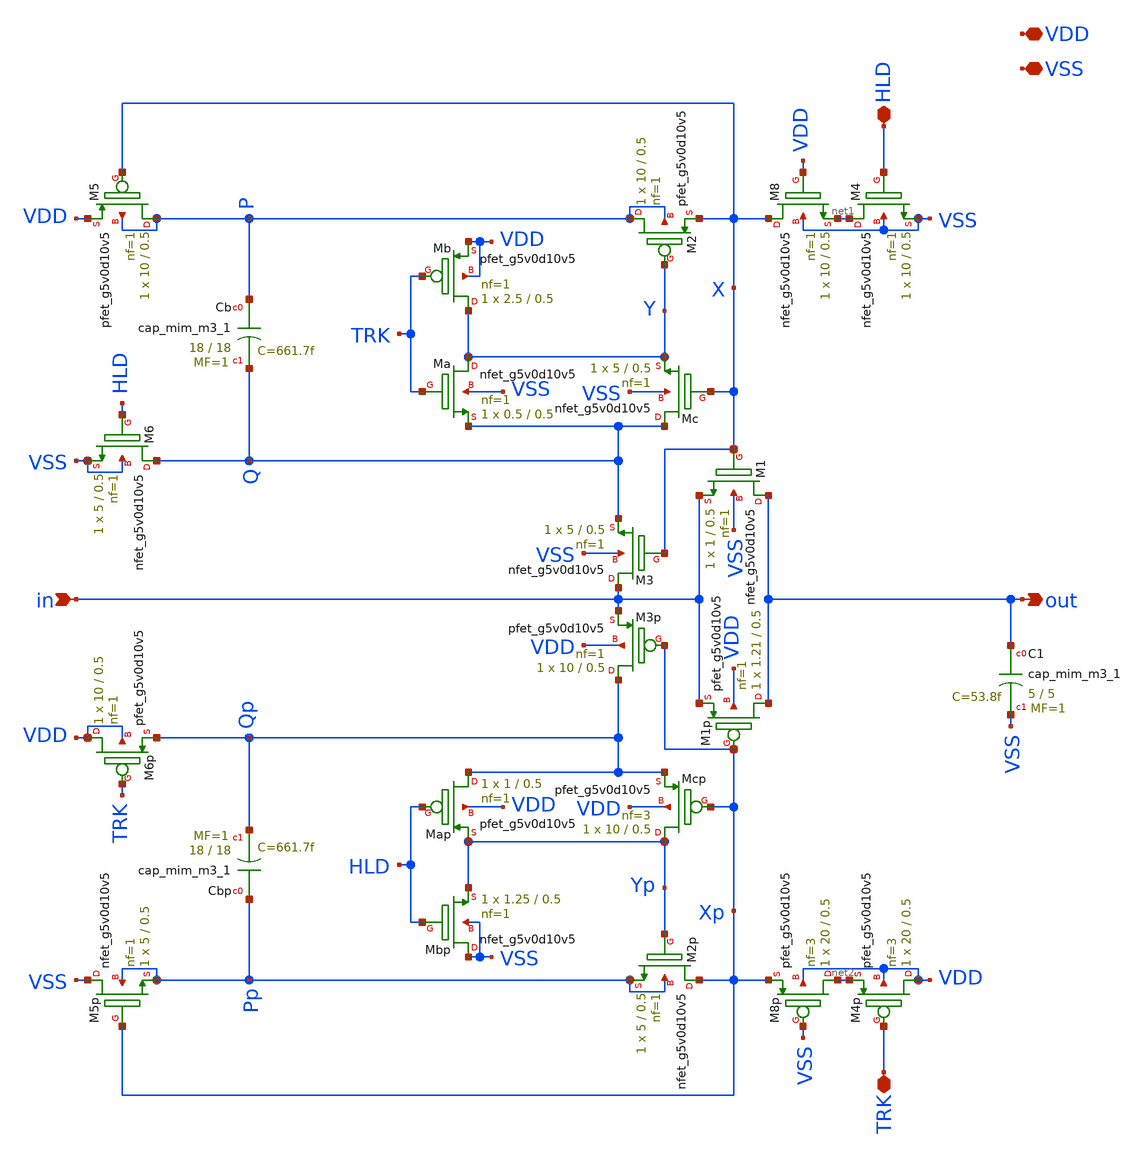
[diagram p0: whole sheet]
** sch_path: xschem/track_and_hold/track_and_hold.sch
**.subckt track_and_hold VSS VDD in out HLD TRK
*.iopin VSS
*.iopin VDD
*.ipin in
*.opin out
*.iopin HLD
*.iopin TRK
XC1 out VSS sky130_fd_pr__cap_mim_m3_1 W=5 L=5 MF=1 m=1
XM1 out X in VSS sky130_fd_pr__nfet_g5v0d10v5 L=0.5 W=1 nf=1 ad='int((nf+1)/2) * W/nf * 0.29' as='int((nf+2)/2) * W/nf * 0.29'
+ pd='2*int((nf+1)/2) * (W/nf + 0.29)' ps='2*int((nf+2)/2) * (W/nf + 0.29)' nrd='0.29 / W' nrs='0.29 / W'
+ sa=0 sb=0 sd=0 mult=1 m=1
XM1p out Xp in VDD sky130_fd_pr__pfet_g5v0d10v5 L=0.5 W=1.21 nf=1 ad='int((nf+1)/2) * W/nf * 0.29' as='int((nf+2)/2) * W/nf * 0.29'
+ pd='2*int((nf+1)/2) * (W/nf + 0.29)' ps='2*int((nf+2)/2) * (W/nf + 0.29)' nrd='0.29 / W' nrs='0.29 / W'
+ sa=0 sb=0 sd=0 mult=1 m=1
XM4 net1 HLD VSS VSS sky130_fd_pr__nfet_g5v0d10v5 L=0.5 W=10 nf=1 ad='int((nf+1)/2) * W/nf * 0.29' as='int((nf+2)/2) * W/nf * 0.29'
+ pd='2*int((nf+1)/2) * (W/nf + 0.29)' ps='2*int((nf+2)/2) * (W/nf + 0.29)' nrd='0.29 / W' nrs='0.29 / W'
+ sa=0 sb=0 sd=0 mult=1 m=1
XM2 P Y X P sky130_fd_pr__pfet_g5v0d10v5 L=0.5 W=10 nf=1 ad='int((nf+1)/2) * W/nf * 0.29' as='int((nf+2)/2) * W/nf * 0.29'
+ pd='2*int((nf+1)/2) * (W/nf + 0.29)' ps='2*int((nf+2)/2) * (W/nf + 0.29)' nrd='0.29 / W' nrs='0.29 / W'
+ sa=0 sb=0 sd=0 mult=1 m=1
XM3 in X Q VSS sky130_fd_pr__nfet_g5v0d10v5 L=0.5 W=5 nf=1 ad='int((nf+1)/2) * W/nf * 0.29' as='int((nf+2)/2) * W/nf * 0.29'
+ pd='2*int((nf+1)/2) * (W/nf + 0.29)' ps='2*int((nf+2)/2) * (W/nf + 0.29)' nrd='0.29 / W' nrs='0.29 / W'
+ sa=0 sb=0 sd=0 mult=1 m=1
XM6 Q HLD VSS VSS sky130_fd_pr__nfet_g5v0d10v5 L=0.5 W=5 nf=1 ad='int((nf+1)/2) * W/nf * 0.29' as='int((nf+2)/2) * W/nf * 0.29'
+ pd='2*int((nf+1)/2) * (W/nf + 0.29)' ps='2*int((nf+2)/2) * (W/nf + 0.29)' nrd='0.29 / W' nrs='0.29 / W'
+ sa=0 sb=0 sd=0 mult=1 m=1
XM3p Qp Xp in VDD sky130_fd_pr__pfet_g5v0d10v5 L=0.5 W=10 nf=1 ad='int((nf+1)/2) * W/nf * 0.29' as='int((nf+2)/2) * W/nf * 0.29'
+ pd='2*int((nf+1)/2) * (W/nf + 0.29)' ps='2*int((nf+2)/2) * (W/nf + 0.29)' nrd='0.29 / W' nrs='0.29 / W'
+ sa=0 sb=0 sd=0 mult=1 m=1
XM5 P X VDD P sky130_fd_pr__pfet_g5v0d10v5 L=0.5 W=10 nf=1 ad='int((nf+1)/2) * W/nf * 0.29' as='int((nf+2)/2) * W/nf * 0.29'
+ pd='2*int((nf+1)/2) * (W/nf + 0.29)' ps='2*int((nf+2)/2) * (W/nf + 0.29)' nrd='0.29 / W' nrs='0.29 / W'
+ sa=0 sb=0 sd=0 mult=1 m=1
XCb P Q sky130_fd_pr__cap_mim_m3_1 W=18 L=18 MF=1 m=1
XM8 X VDD net1 VSS sky130_fd_pr__nfet_g5v0d10v5 L=0.5 W=10 nf=1 ad='int((nf+1)/2) * W/nf * 0.29' as='int((nf+2)/2) * W/nf * 0.29'
+ pd='2*int((nf+1)/2) * (W/nf + 0.29)' ps='2*int((nf+2)/2) * (W/nf + 0.29)' nrd='0.29 / W' nrs='0.29 / W'
+ sa=0 sb=0 sd=0 mult=1 m=1
XMb Y TRK VDD VDD sky130_fd_pr__pfet_g5v0d10v5 L=0.5 W=2.5 nf=1 ad='int((nf+1)/2) * W/nf * 0.29' as='int((nf+2)/2) * W/nf * 0.29'
+ pd='2*int((nf+1)/2) * (W/nf + 0.29)' ps='2*int((nf+2)/2) * (W/nf + 0.29)' nrd='0.29 / W' nrs='0.29 / W'
+ sa=0 sb=0 sd=0 mult=1 m=1
XMa Y TRK Q VSS sky130_fd_pr__nfet_g5v0d10v5 L=0.5 W=0.5 nf=1 ad='int((nf+1)/2) * W/nf * 0.29' as='int((nf+2)/2) * W/nf * 0.29'
+ pd='2*int((nf+1)/2) * (W/nf + 0.29)' ps='2*int((nf+2)/2) * (W/nf + 0.29)' nrd='0.29 / W' nrs='0.29 / W'
+ sa=0 sb=0 sd=0 mult=1 m=1
XMc Q X Y VSS sky130_fd_pr__nfet_g5v0d10v5 L=0.5 W=5 nf=1 ad='int((nf+1)/2) * W/nf * 0.29' as='int((nf+2)/2) * W/nf * 0.29'
+ pd='2*int((nf+1)/2) * (W/nf + 0.29)' ps='2*int((nf+2)/2) * (W/nf + 0.29)' nrd='0.29 / W' nrs='0.29 / W'
+ sa=0 sb=0 sd=0 mult=1 m=1
XCbp Pp Qp sky130_fd_pr__cap_mim_m3_1 W=18 L=18 MF=1 m=1
XM6p VDD TRK Qp VDD sky130_fd_pr__pfet_g5v0d10v5 L=0.5 W=10 nf=1 ad='int((nf+1)/2) * W/nf * 0.29' as='int((nf+2)/2) * W/nf * 0.29'
+ pd='2*int((nf+1)/2) * (W/nf + 0.29)' ps='2*int((nf+2)/2) * (W/nf + 0.29)' nrd='0.29 / W' nrs='0.29 / W'
+ sa=0 sb=0 sd=0 mult=1 m=1
XM5p VSS Xp Pp Pp sky130_fd_pr__nfet_g5v0d10v5 L=0.5 W=5 nf=1 ad='int((nf+1)/2) * W/nf * 0.29' as='int((nf+2)/2) * W/nf * 0.29'
+ pd='2*int((nf+1)/2) * (W/nf + 0.29)' ps='2*int((nf+2)/2) * (W/nf + 0.29)' nrd='0.29 / W' nrs='0.29 / W'
+ sa=0 sb=0 sd=0 mult=1 m=1
XM2p Xp Yp Pp Pp sky130_fd_pr__nfet_g5v0d10v5 L=0.5 W=5 nf=1 ad='int((nf+1)/2) * W/nf * 0.29' as='int((nf+2)/2) * W/nf * 0.29'
+ pd='2*int((nf+1)/2) * (W/nf + 0.29)' ps='2*int((nf+2)/2) * (W/nf + 0.29)' nrd='0.29 / W' nrs='0.29 / W'
+ sa=0 sb=0 sd=0 mult=1 m=1
XMcp Yp Xp Qp VDD sky130_fd_pr__pfet_g5v0d10v5 L=0.5 W=10 nf=3 ad='int((nf+1)/2) * W/nf * 0.29' as='int((nf+2)/2) * W/nf * 0.29'
+ pd='2*int((nf+1)/2) * (W/nf + 0.29)' ps='2*int((nf+2)/2) * (W/nf + 0.29)' nrd='0.29 / W' nrs='0.29 / W'
+ sa=0 sb=0 sd=0 mult=1 m=1
XMap Qp HLD Yp VDD sky130_fd_pr__pfet_g5v0d10v5 L=0.5 W=1 nf=1 ad='int((nf+1)/2) * W/nf * 0.29' as='int((nf+2)/2) * W/nf * 0.29'
+ pd='2*int((nf+1)/2) * (W/nf + 0.29)' ps='2*int((nf+2)/2) * (W/nf + 0.29)' nrd='0.29 / W' nrs='0.29 / W'
+ sa=0 sb=0 sd=0 mult=1 m=1
XMbp VSS HLD Yp VSS sky130_fd_pr__nfet_g5v0d10v5 L=0.5 W=1.25 nf=1 ad='int((nf+1)/2) * W/nf * 0.29' as='int((nf+2)/2) * W/nf * 0.29'
+ pd='2*int((nf+1)/2) * (W/nf + 0.29)' ps='2*int((nf+2)/2) * (W/nf + 0.29)' nrd='0.29 / W' nrs='0.29 / W'
+ sa=0 sb=0 sd=0 mult=1 m=1
XM8p net2 VSS Xp VDD sky130_fd_pr__pfet_g5v0d10v5 L=0.5 W=20 nf=3 ad='int((nf+1)/2) * W/nf * 0.29' as='int((nf+2)/2) * W/nf * 0.29'
+ pd='2*int((nf+1)/2) * (W/nf + 0.29)' ps='2*int((nf+2)/2) * (W/nf + 0.29)' nrd='0.29 / W' nrs='0.29 / W'
+ sa=0 sb=0 sd=0 mult=1 m=1
XM4p VDD TRK net2 VDD sky130_fd_pr__pfet_g5v0d10v5 L=0.5 W=20 nf=3 ad='int((nf+1)/2) * W/nf * 0.29' as='int((nf+2)/2) * W/nf * 0.29'
+ pd='2*int((nf+1)/2) * (W/nf + 0.29)' ps='2*int((nf+2)/2) * (W/nf + 0.29)' nrd='0.29 / W' nrs='0.29 / W'
+ sa=0 sb=0 sd=0 mult=1 m=1
**.ends
.end
